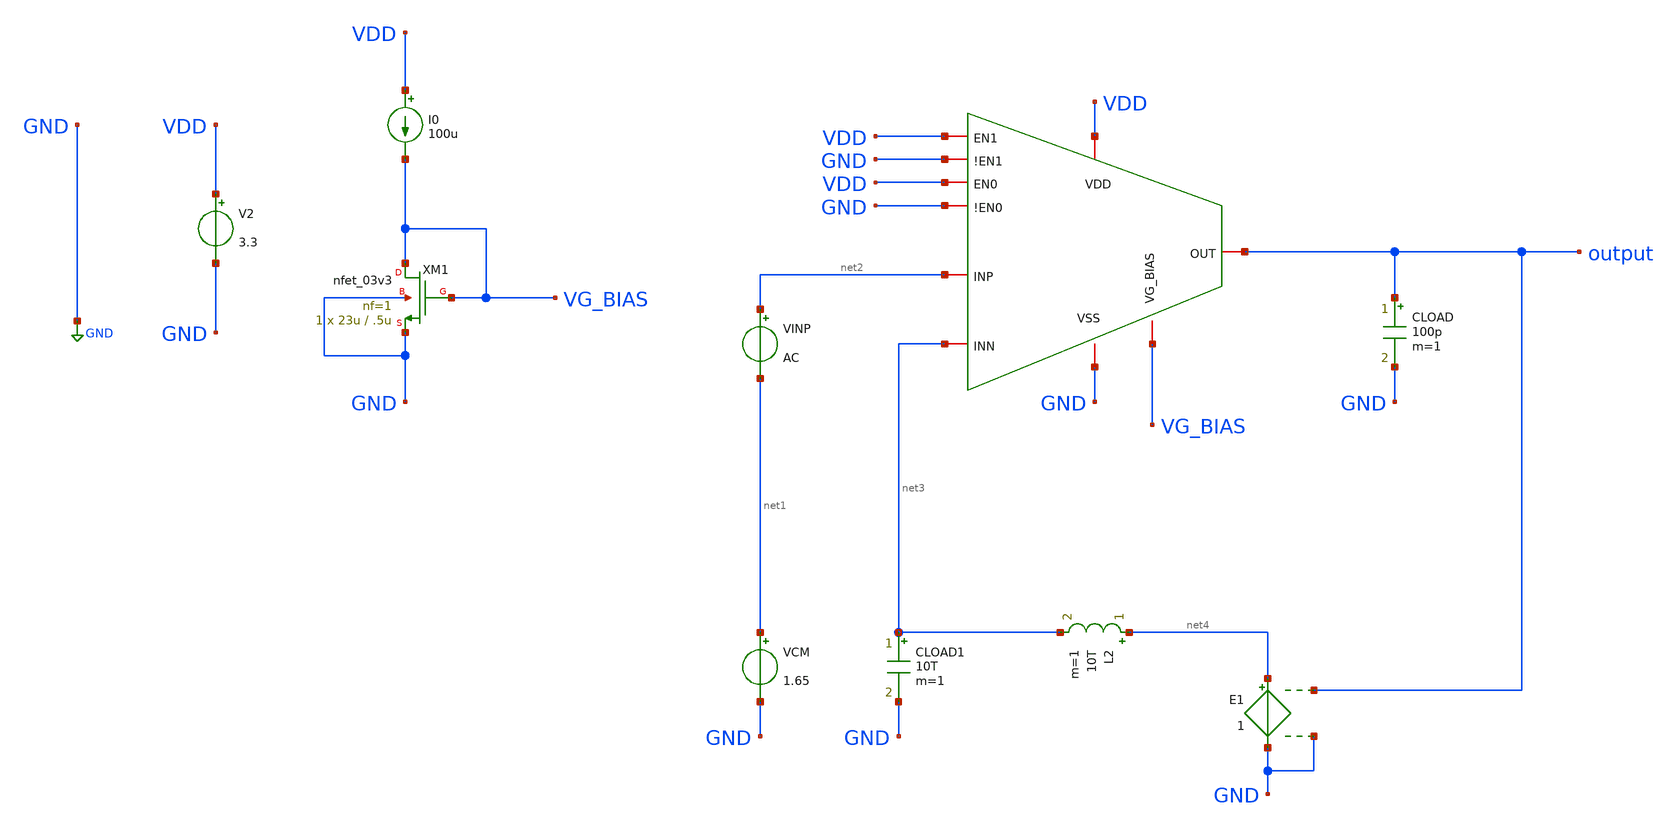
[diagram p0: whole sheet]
** sch_path: designs/libs/core_amps/ota_folded_cascode/programmable_ac_open_loop_tb.sch
**.subckt programmable_ac_open_loop_tb
x1 VDD VDD GND GND VDD GND net3 net2 output VG_BIAS programmable_folded
XM1 VG_BIAS VG_BIAS GND GND nfet_03v3 L=.5u W=23u nf=1 ad='int((nf+1)/2) * W/nf * 0.18u' as='int((nf+2)/2) * W/nf * 0.18u'
+ pd='2*int((nf+1)/2) * (W/nf + 0.18u)' ps='2*int((nf+2)/2) * (W/nf + 0.18u)' nrd='0.18u / W' nrs='0.18u / W'
+ sa=0 sb=0 sd=0 m=1
I0 VDD VG_BIAS 100u
V2 VDD GND 3.3
VINP net2 net1 AC
VCM net1 GND 1.65
L2 net4 net3 10T m=1
CLOAD1 net3 GND 10T m=1
E1 net4 GND output GND 1
CLOAD output GND 100p m=1
**** begin user architecture code

.include $::180MCU_MODELS/design.ngspice
.lib $::180MCU_MODELS/sm141064.ngspice typical



.control
ac dec 100 1 1G

plot vdb(output) ph(v(output))*180/3.14159

meas ac dc_gain find vdb(output) at=100
let bw_level = dc_gain - 3
meas ac bw when vdb(output) = bw_level fall=1

.endc



**** end user architecture code
**.ends
.GLOBAL GND
.end
